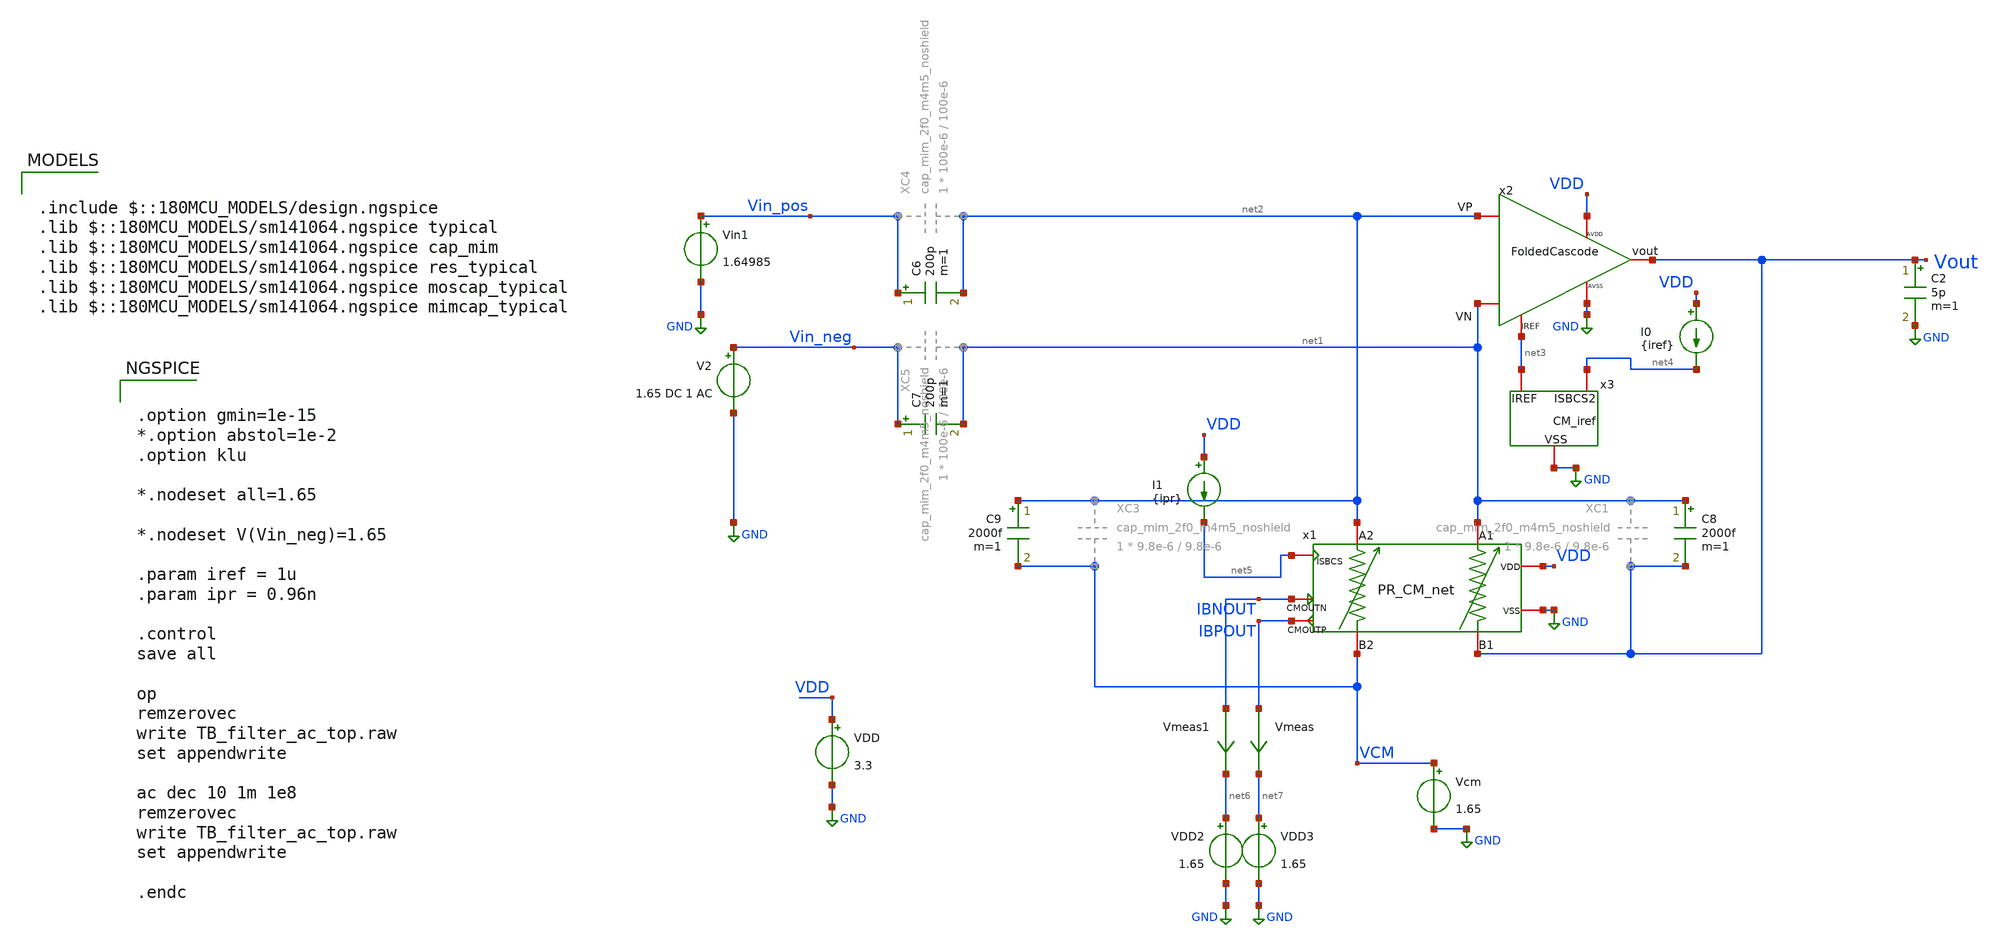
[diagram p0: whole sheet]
** sch_path: TIA_Filter/TB_filter_ac_top.sch
**.subckt TB_filter_ac_top
C2 Vout GND 5p m=1
Vin1 Vin_pos GND 1.64985
V2 Vin_neg GND 1.65 DC 1 AC
x1 net5 net1 net2 VCM Vout IBNOUT IBPOUT VDD GND PR_CM_net
x2 net2 net1 Vout net3 VDD GND FoldedCascode
x3 net4 net3 GND CM_iref
I0 VDD net4 {iref}
I1 VDD net5 {ipr}
Vmeas IBPOUT net7 0
.save i(vmeas)
Vmeas1 IBNOUT net6 0
.save i(vmeas1)
Vcm VCM GND 1.65
VDD2 net6 GND 1.65
VDD3 net7 GND 1.65
VDD VDD GND 3.3
C6 Vin_pos net2 200p m=1
C7 Vin_neg net1 200p m=1
C8 net1 Vout 2000f m=1
C9 net2 VCM 2000f m=1
**** begin user architecture code

.include $::180MCU_MODELS/design.ngspice
.lib $::180MCU_MODELS/sm141064.ngspice typical
.lib $::180MCU_MODELS/sm141064.ngspice cap_mim
.lib $::180MCU_MODELS/sm141064.ngspice res_typical
.lib $::180MCU_MODELS/sm141064.ngspice moscap_typical
.lib $::180MCU_MODELS/sm141064.ngspice mimcap_typical



.option gmin=1e-15
*.option abstol=1e-2
.option klu

*.nodeset all=1.65

*.nodeset V(Vin_neg)=1.65

.param iref = 1u
.param ipr = 0.96n

.control
save all

op
remzerovec
write TB_filter_ac_top.raw
set appendwrite

ac dec 10 1m 1e8
remzerovec
write TB_filter_ac_top.raw
set appendwrite

.endc


**** end user architecture code
**.ends
.GLOBAL GND
.end
